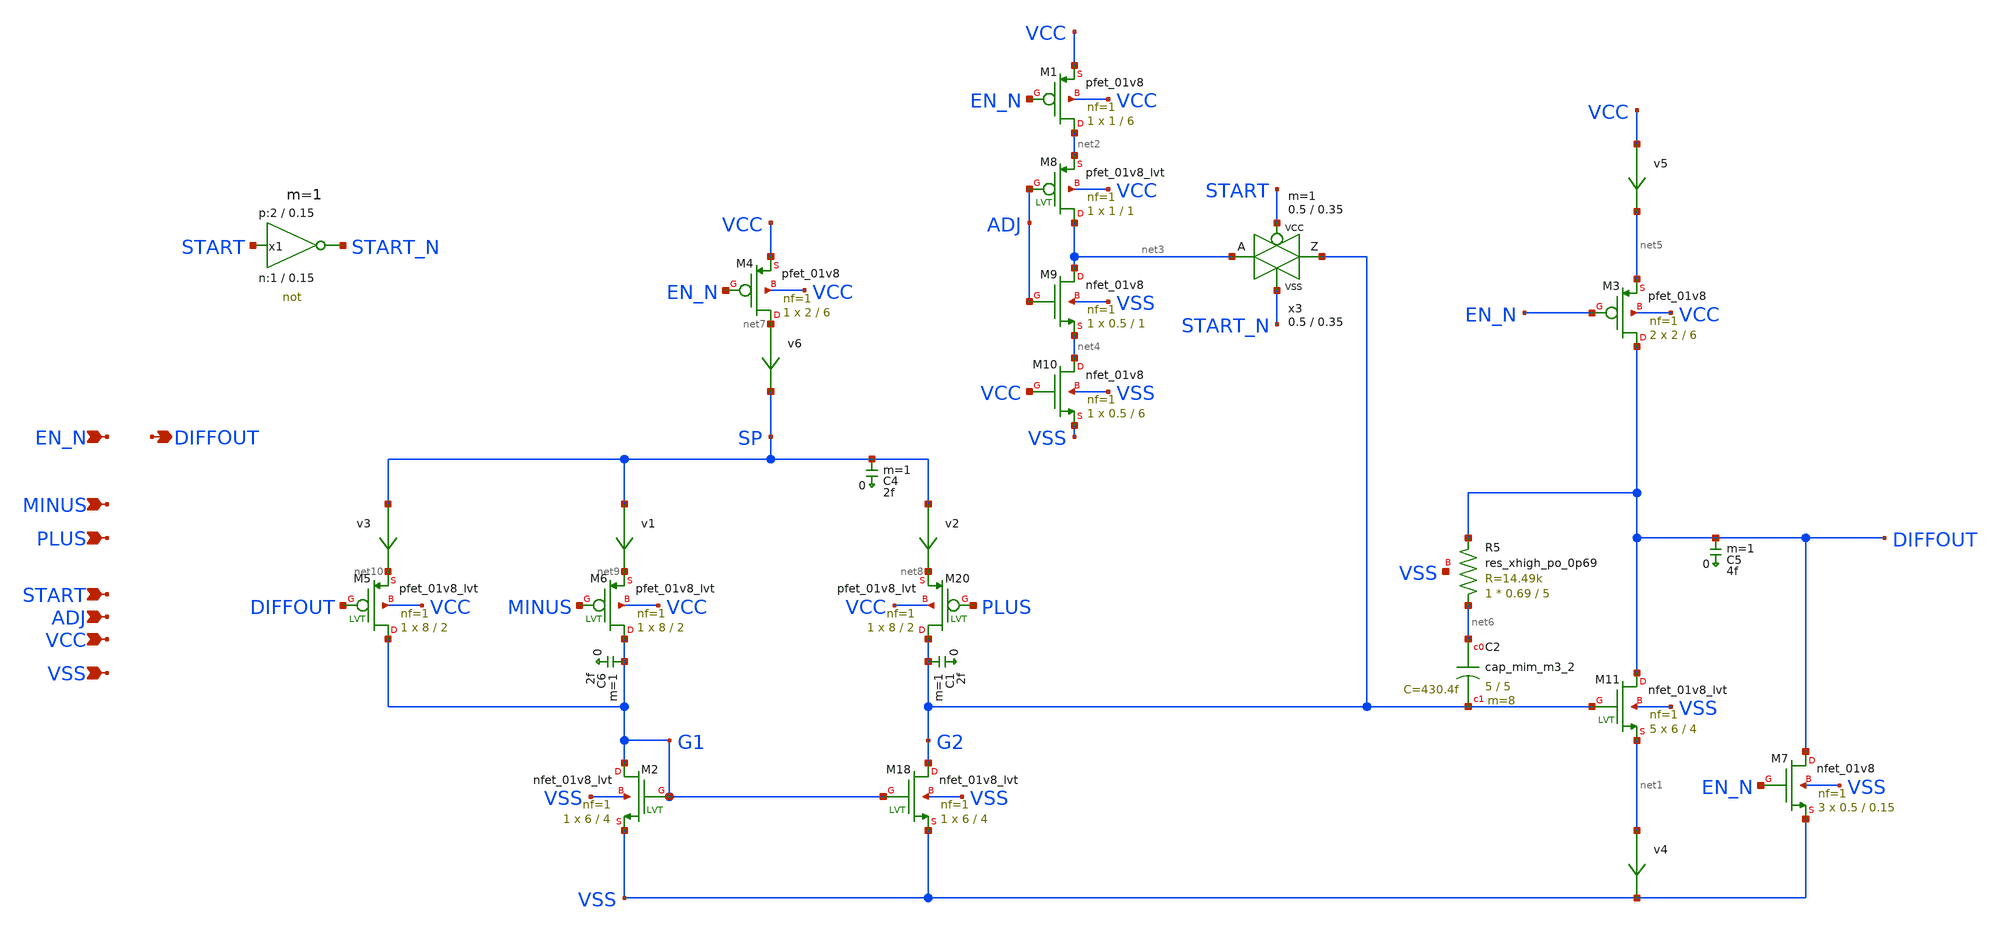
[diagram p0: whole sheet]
** sch_path: sky130_tests/bandgap_opamp.sch
* Copyright 2021 Stefan Frederik Schippers
* Licensed under the Apache License, Version 2.0 (the "License");
* you may not use this file except in compliance with the License.
* You may obtain a copy of the License at
* https://www.apache.org/licenses/LICENSE-2.0
* Unless required by applicable law or agreed to in writing, software
* distributed under the License is distributed on an "AS IS" BASIS,
* WITHOUT WARRANTIES OR CONDITIONS OF ANY KIND, either express or implied.
* See the License for the specific language governing permissions and
* limitations under the License.
* sky130_tests/not.sym:
* Copyright 2020 Stefan Frederik Schippers
**.subckt bandgap_opamp PLUS MINUS EN_N VSS VCC DIFFOUT ADJ START
*.ipin PLUS
*.ipin MINUS
*.ipin EN_N
*.ipin VSS
*.ipin VCC
*.opin DIFFOUT
*.ipin ADJ
*.ipin START
C6 G1 0 2f m=1
XM4 net7 EN_N VCC VCC sky130_fd_pr__pfet_01v8 L=6 W=2 nf=1 ad='int((1 + 1)/2) * 2 / 1 * 0.29' as='int((1 + 2)/2) * 2 / 1 * 0.29'
+ pd='2*int((1 + 1)/2) * (2 / 1 + 0.29)' ps='2*int((1 + 2)/2) * (2 / 1 + 0.29)' nrd='0.29 / 2 ' nrs='0.29 / 2 '
+ sa=0 sb=0 sd=0 mult=1 m=1
XM18 G2 G1 VSS VSS sky130_fd_pr__nfet_01v8_lvt L=4 W=6 nf=1 ad='int((1 + 1)/2) * 6 / 1 * 0.29' as='int((1 + 2)/2) * 6 / 1 * 0.29'
+ pd='2*int((1 + 1)/2) * (6 / 1 + 0.29)' ps='2*int((1 + 2)/2) * (6 / 1 + 0.29)' nrd='0.29 / 6 ' nrs='0.29 / 6 '
+ sa=0 sb=0 sd=0 mult=1 m=1
XM2 G1 G1 VSS VSS sky130_fd_pr__nfet_01v8_lvt L=4 W=6 nf=1 ad='int((1 + 1)/2) * 6 / 1 * 0.29' as='int((1 + 2)/2) * 6 / 1 * 0.29'
+ pd='2*int((1 + 1)/2) * (6 / 1 + 0.29)' ps='2*int((1 + 2)/2) * (6 / 1 + 0.29)' nrd='0.29 / 6 ' nrs='0.29 / 6 '
+ sa=0 sb=0 sd=0 mult=1 m=1
XM20 G2 PLUS net8 VCC sky130_fd_pr__pfet_01v8_lvt L=2 W=8 nf=1 ad='int((1 + 1)/2) * 8 / 1 * 0.29' as='int((1 + 2)/2) * 8 / 1 * 0.29'
+ pd='2*int((1 + 1)/2) * (8 / 1 + 0.29)' ps='2*int((1 + 2)/2) * (8 / 1 + 0.29)' nrd='0.29 / 8 ' nrs='0.29 / 8 '
+ sa=0 sb=0 sd=0 mult=1 m=1
XM6 G1 MINUS net9 VCC sky130_fd_pr__pfet_01v8_lvt L=2 W=8 nf=1 ad='int((1 + 1)/2) * 8 / 1 * 0.29' as='int((1 + 2)/2) * 8 / 1 * 0.29'
+ pd='2*int((1 + 1)/2) * (8 / 1 + 0.29)' ps='2*int((1 + 2)/2) * (8 / 1 + 0.29)' nrd='0.29 / 8 ' nrs='0.29 / 8 '
+ sa=0 sb=0 sd=0 mult=1 m=1
v1 SP net9 0
.save i(v1)
C4 SP 0 2f m=1
C1 G2 0 2f m=1
C5 DIFFOUT 0 4f m=1
XM11 DIFFOUT G2 net1 VSS sky130_fd_pr__nfet_01v8_lvt L=4 W=6 nf=1 ad='int((1 + 1)/2) * 6 / 1 * 0.29'
+ as='int((1 + 2)/2) * 6 / 1 * 0.29' pd='2*int((1 + 1)/2) * (6 / 1 + 0.29)' ps='2*int((1 + 2)/2) * (6 / 1 + 0.29)'
+ nrd='0.29 / 6 ' nrs='0.29 / 6 ' sa=0 sb=0 sd=0 mult=5 m=5
v2 SP net8 0
.save i(v2)
XM5 G1 DIFFOUT net10 VCC sky130_fd_pr__pfet_01v8_lvt L=2 W=8 nf=1 ad='int((1 + 1)/2) * 8 / 1 * 0.29'
+ as='int((1 + 2)/2) * 8 / 1 * 0.29' pd='2*int((1 + 1)/2) * (8 / 1 + 0.29)' ps='2*int((1 + 2)/2) * (8 / 1 + 0.29)'
+ nrd='0.29 / 8 ' nrs='0.29 / 8 ' sa=0 sb=0 sd=0 mult=1 m=1
v3 SP net10 0
.save i(v3)
v4 net1 VSS 0
.save i(v4)
v5 VCC net5 0
.save i(v5)
v6 net7 SP 0
.save i(v6)
XM7 DIFFOUT EN_N VSS VSS sky130_fd_pr__nfet_01v8 L=0.15 W=0.5 nf=1 ad='int((1 + 1)/2) * 0.5 / 1 * 0.29'
+ as='int((1 + 2)/2) * 0.5 / 1 * 0.29' pd='2*int((1 + 1)/2) * (0.5 / 1 + 0.29)' ps='2*int((1 + 2)/2) * (0.5 / 1 + 0.29)'
+ nrd='0.29 / 0.5 ' nrs='0.29 / 0.5 ' sa=0 sb=0 sd=0 mult=3 m=3
XM1 net2 EN_N VCC VCC sky130_fd_pr__pfet_01v8 L=6 W=1 nf=1 ad='int((1 + 1)/2) * 1 / 1 * 0.29' as='int((1 + 2)/2) * 1 / 1 * 0.29'
+ pd='2*int((1 + 1)/2) * (1 / 1 + 0.29)' ps='2*int((1 + 2)/2) * (1 / 1 + 0.29)' nrd='0.29 / 1 ' nrs='0.29 / 1 '
+ sa=0 sb=0 sd=0 mult=1 m=1
XM8 net3 ADJ net2 VCC sky130_fd_pr__pfet_01v8_lvt L=1 W=1 nf=1 ad='int((1 + 1)/2) * 1 / 1 * 0.29' as='int((1 + 2)/2) * 1 / 1 * 0.29'
+ pd='2*int((1 + 1)/2) * (1 / 1 + 0.29)' ps='2*int((1 + 2)/2) * (1 / 1 + 0.29)' nrd='0.29 / 1 ' nrs='0.29 / 1 '
+ sa=0 sb=0 sd=0 mult=1 m=1
XM9 net3 ADJ net4 VSS sky130_fd_pr__nfet_01v8 L=1 W=0.5 nf=1 ad='int((1 + 1)/2) * 0.5 / 1 * 0.29' as='int((1 + 2)/2) * 0.5 / 1 * 0.29'
+ pd='2*int((1 + 1)/2) * (0.5 / 1 + 0.29)' ps='2*int((1 + 2)/2) * (0.5 / 1 + 0.29)' nrd='0.29 / 0.5 ' nrs='0.29 / 0.5 '
+ sa=0 sb=0 sd=0 mult=1 m=1
XM10 net4 VCC VSS VSS sky130_fd_pr__nfet_01v8 L=6 W=0.5 nf=1 ad='int((1 + 1)/2) * 0.5 / 1 * 0.29' as='int((1 + 2)/2) * 0.5 / 1 * 0.29'
+ pd='2*int((1 + 1)/2) * (0.5 / 1 + 0.29)' ps='2*int((1 + 2)/2) * (0.5 / 1 + 0.29)' nrd='0.29 / 0.5 ' nrs='0.29 / 0.5 '
+ sa=0 sb=0 sd=0 mult=1 m=1
x1 START_N START VCC VSS not W_N=1 L_N=0.15 W_P=2 L_P=0.15 m=1
x3 G2 net3 START START_N VCC VSS passgate_nlvt W_N=0.5 L_N=0.35 W_P=0.5 L_P=0.35 ad=0 as=0 pd=0 ps=1
XM3 DIFFOUT EN_N net5 VCC sky130_fd_pr__pfet_01v8 L=6 W=2 nf=1 ad='int((1 + 1)/2) * 2 / 1 * 0.29' as='int((1 + 2)/2) * 2 / 1 * 0.29'
+ pd='2*int((1 + 1)/2) * (2 / 1 + 0.29)' ps='2*int((1 + 2)/2) * (2 / 1 + 0.29)' nrd='0.29 / 2 ' nrs='0.29 / 2 '
+ sa=0 sb=0 sd=0 mult=2 m=2
XC2 net6 G2 sky130_fd_pr__cap_mim_m3_2 W=5 L=5 MF=8 m=8
XR5 net6 DIFFOUT VSS sky130_fd_pr__res_xhigh_po_0p69 L=5 mult=1 m=1
**.ends

* expanding   symbol:  sky130_tests/not.sym # of pins=2
** sym_path: sky130_tests/not.sym
** sch_path: sky130_tests/not.sch
.subckt not y a VCCPIN VSSPIN     W_N=1 L_N=0.15 W_P=2 L_P=0.15
*.opin y
*.ipin a
XM1 DN a VSSPIN VSSPIN sky130_fd_pr__nfet_01v8 L=L_N W=W_N nf=1 ad='int((1 + 1)/2) * W_N / 1 * 0.29'
+ as='int((1 + 2)/2) * W_N / 1 * 0.29' pd='2*int((1 + 1)/2) * (W_N / 1 + 0.29)' ps='2*int((1 + 2)/2) * (W_N / 1 + 0.29)'
+ nrd='0.29 / W_N ' nrs='0.29 / W_N ' sa=0 sb=0 sd=0 mult=1 m=1
XM2 DP a VCCPIN VCCPIN sky130_fd_pr__pfet_01v8 L=L_P W=W_P nf=1 ad='int((1 + 1)/2) * W_P / 1 * 0.29'
+ as='int((1 + 2)/2) * W_P / 1 * 0.29' pd='2*int((1 + 1)/2) * (W_P / 1 + 0.29)' ps='2*int((1 + 2)/2) * (W_P / 1 + 0.29)'
+ nrd='0.29 / W_P ' nrs='0.29 / W_P ' sa=0 sb=0 sd=0 mult=1 m=1
Vmeas DP y 0
.save i(vmeas)
Vmeas1 y DN 0
.save i(vmeas1)
.save v(dp)
.save v(dn)
.ends


* expanding   symbol:  sky130_tests/passgate_nlvt.sym # of pins=4
** sym_path: sky130_tests/passgate_nlvt.sym
** sch_path: sky130_tests/passgate_nlvt.sch
.subckt passgate_nlvt Z A GP GN VCCBPIN VSSBPIN  W_N=1 L_N=0.2 W_P=1 L_P=0.2   ad=0 as=0 pd=0 ps=0
*.iopin A
*.iopin Z
*.ipin GP
*.ipin GN
XM1 Z GN A VSSBPIN sky130_fd_pr__nfet_01v8_lvt L=L_N W=W_N nf=1 ad='int((1 + 1)/2) * W_N / 1 * 0.29'
+ as='int((1 + 2)/2) * W_N / 1 * 0.29' pd='2*int((1 + 1)/2) * (W_N / 1 + 0.29)' ps='2*int((1 + 2)/2) * (W_N / 1 + 0.29)'
+ nrd='0.29 / W_N ' nrs='0.29 / W_N ' sa=0 sb=0 sd=0 mult=1 m=1
XM2 Z GP A VCCBPIN sky130_fd_pr__pfet_01v8_lvt L=L_P W=W_P nf=1 ad='int((1 + 1)/2) * W_P / 1 * 0.29'
+ as='int((1 + 2)/2) * W_P / 1 * 0.29' pd='2*int((1 + 1)/2) * (W_P / 1 + 0.29)' ps='2*int((1 + 2)/2) * (W_P / 1 + 0.29)'
+ nrd='0.29 / W_P ' nrs='0.29 / W_P ' sa=0 sb=0 sd=0 mult=1 m=1
* noconn VCCBPIN
* noconn VSSBPIN
.ends

.end
